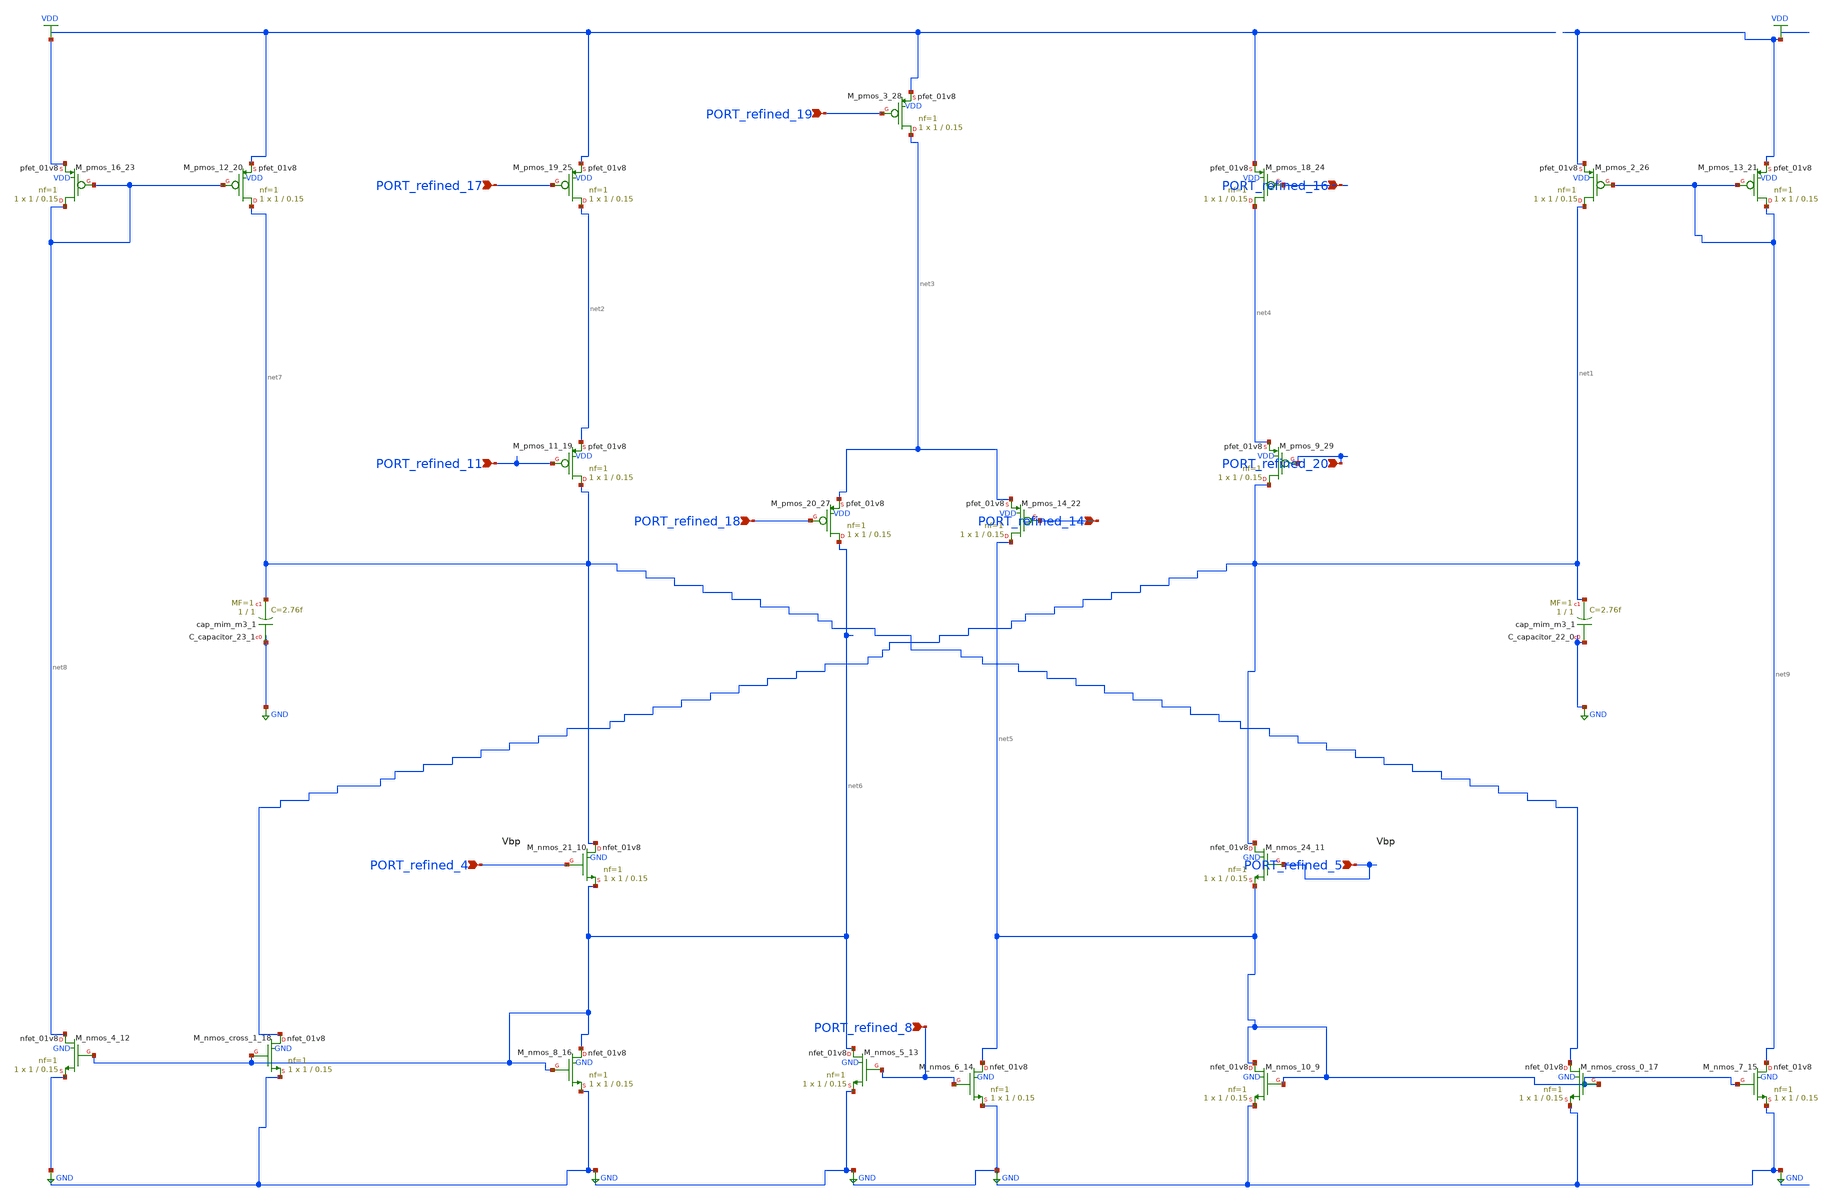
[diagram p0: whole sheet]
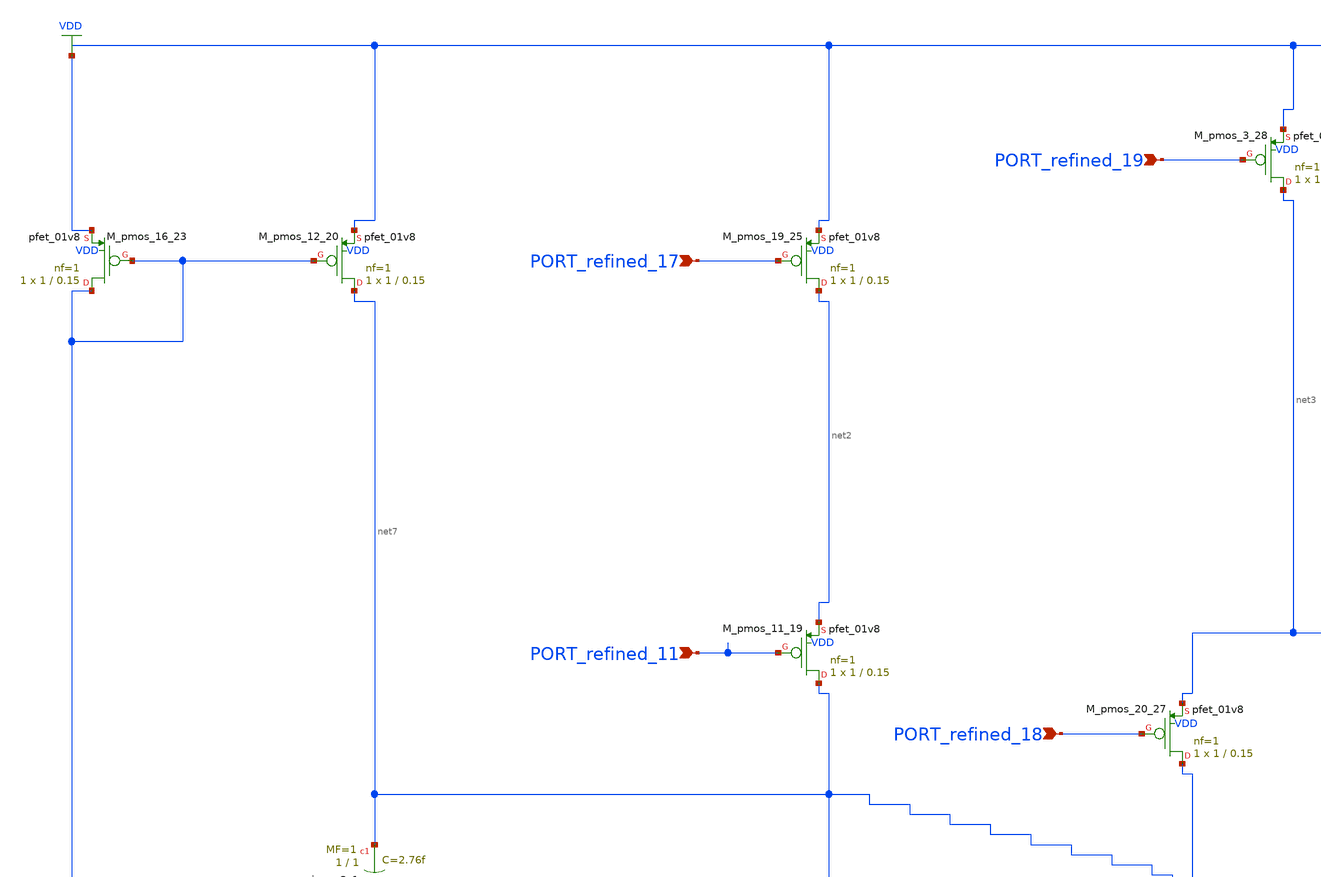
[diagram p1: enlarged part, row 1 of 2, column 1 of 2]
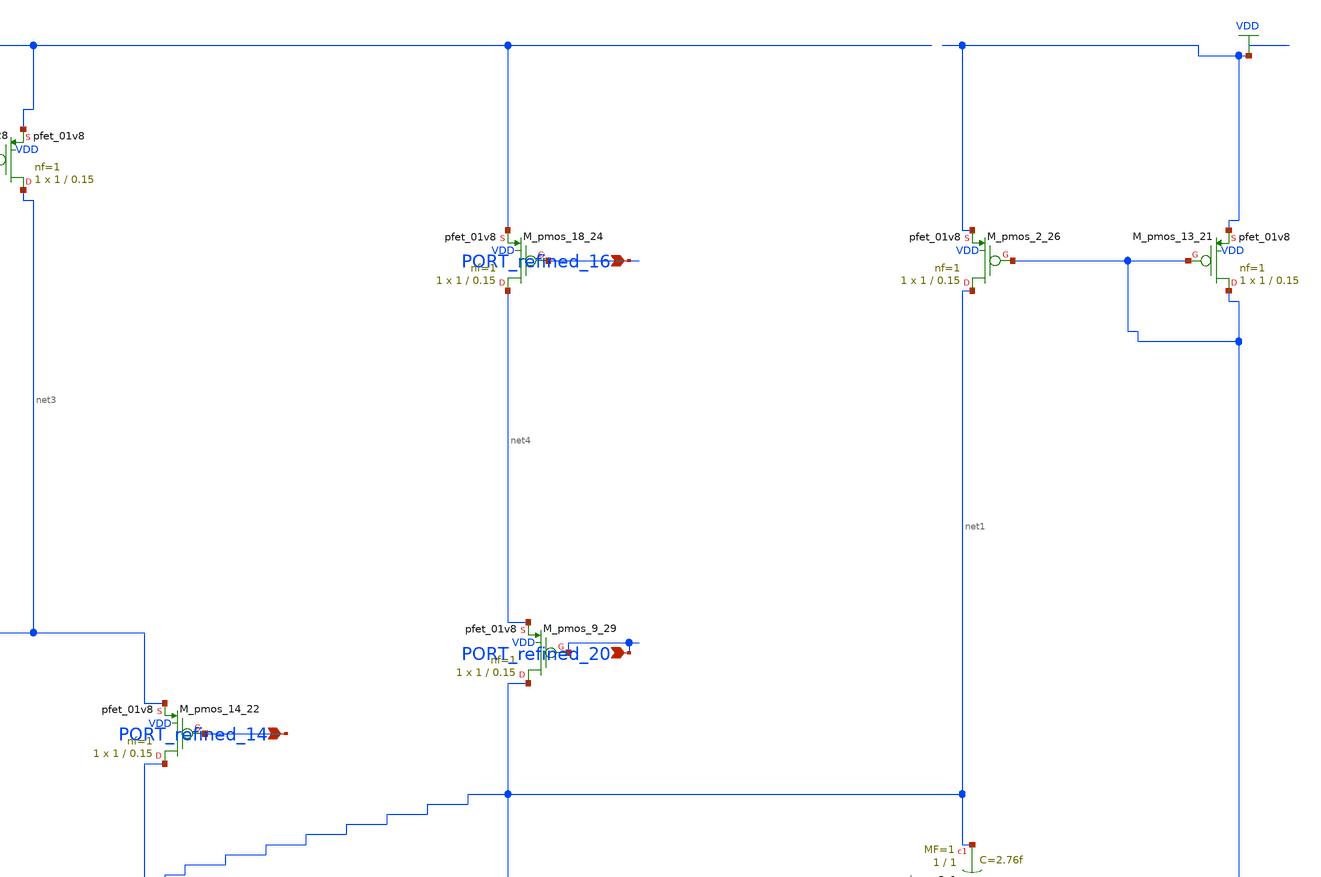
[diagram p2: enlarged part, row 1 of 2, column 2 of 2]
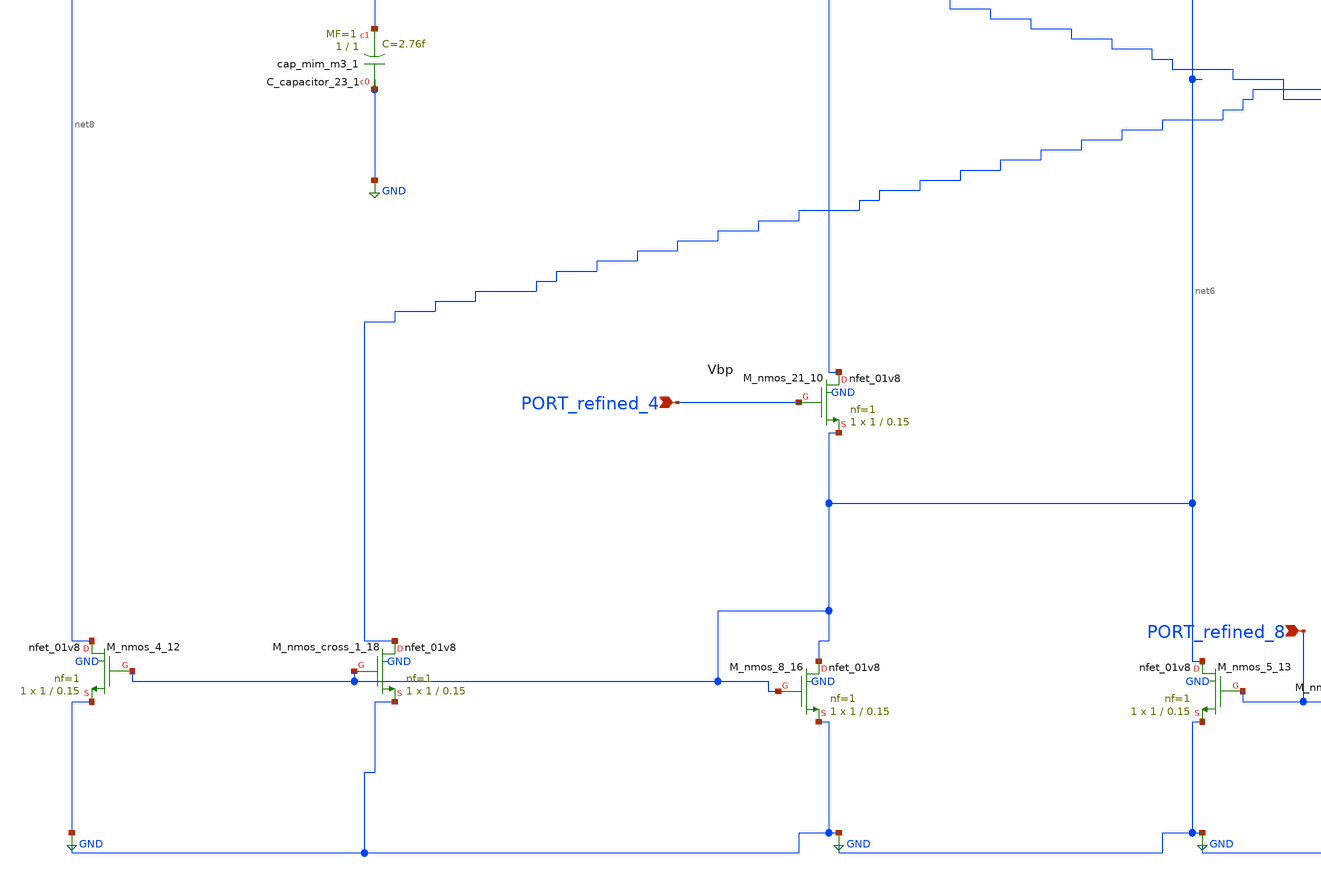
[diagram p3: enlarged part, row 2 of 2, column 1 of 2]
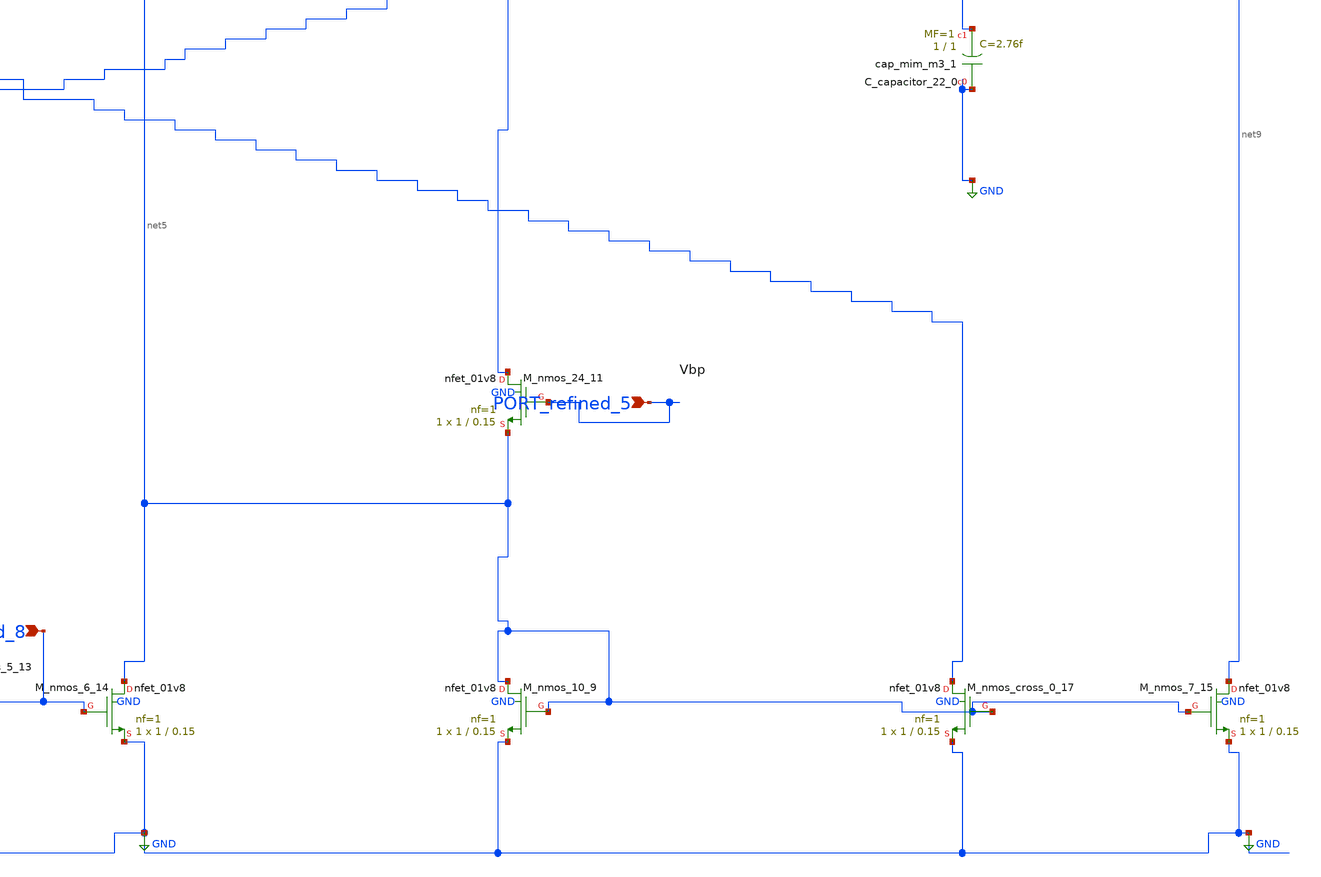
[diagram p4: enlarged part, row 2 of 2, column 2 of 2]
** sch_path: schematics/Image2Net/073.sch
**.subckt 073 PORT_refined_17 PORT_refined_19 PORT_refined_18 PORT_refined_16 PORT_refined_8
*+ PORT_refined_11 PORT_refined_14 PORT_refined_20 PORT_refined_4 PORT_refined_5
*.ipin PORT_refined_17
*.ipin PORT_refined_19
*.ipin PORT_refined_18
*.ipin PORT_refined_16
*.ipin PORT_refined_8
*.ipin PORT_refined_11
*.ipin PORT_refined_14
*.ipin PORT_refined_20
*.ipin PORT_refined_4
*.ipin PORT_refined_5
XC_capacitor_22_0 GND net1 sky130_fd_pr__cap_mim_m3_1 W=1 L=1 MF=1 m=1
XC_capacitor_23_1 GND net7 sky130_fd_pr__cap_mim_m3_1 W=1 L=1 MF=1 m=1
XM_nmos_10_9 net5 net5 GND GND sky130_fd_pr__nfet_01v8 L=0.15 W=1 nf=1 ad='int((1 + 1)/2) * 1 / 1 * 0.29'
+ as='int((1 + 2)/2) * 1 / 1 * 0.29' pd='2*int((1 + 1)/2) * (1 / 1 + 0.29)' ps='2*int((1 + 2)/2) * (1 / 1 + 0.29)'
+ nrd='0.29 / 1 ' nrs='0.29 / 1 ' sa=0 sb=0 sd=0 mult=1 m=1
XM_nmos_21_10 net7 PORT_refined_4 net6 GND sky130_fd_pr__nfet_01v8 L=0.15 W=1 nf=1 ad='int((1 + 1)/2) * 1 / 1 * 0.29'
+ as='int((1 + 2)/2) * 1 / 1 * 0.29' pd='2*int((1 + 1)/2) * (1 / 1 + 0.29)' ps='2*int((1 + 2)/2) * (1 / 1 + 0.29)'
+ nrd='0.29 / 1 ' nrs='0.29 / 1 ' sa=0 sb=0 sd=0 mult=1 m=1
XM_nmos_24_11 net1 PORT_refined_5 net5 GND sky130_fd_pr__nfet_01v8 L=0.15 W=1 nf=1 ad='int((1 + 1)/2) * 1 / 1 * 0.29'
+ as='int((1 + 2)/2) * 1 / 1 * 0.29' pd='2*int((1 + 1)/2) * (1 / 1 + 0.29)' ps='2*int((1 + 2)/2) * (1 / 1 + 0.29)'
+ nrd='0.29 / 1 ' nrs='0.29 / 1 ' sa=0 sb=0 sd=0 mult=1 m=1
XM_nmos_4_12 net8 net6 GND GND sky130_fd_pr__nfet_01v8 L=0.15 W=1 nf=1 ad='int((1 + 1)/2) * 1 / 1 * 0.29'
+ as='int((1 + 2)/2) * 1 / 1 * 0.29' pd='2*int((1 + 1)/2) * (1 / 1 + 0.29)' ps='2*int((1 + 2)/2) * (1 / 1 + 0.29)'
+ nrd='0.29 / 1 ' nrs='0.29 / 1 ' sa=0 sb=0 sd=0 mult=1 m=1
XM_nmos_5_13 net6 PORT_refined_8 GND GND sky130_fd_pr__nfet_01v8 L=0.15 W=1 nf=1 ad='int((1 + 1)/2) * 1 / 1 * 0.29'
+ as='int((1 + 2)/2) * 1 / 1 * 0.29' pd='2*int((1 + 1)/2) * (1 / 1 + 0.29)' ps='2*int((1 + 2)/2) * (1 / 1 + 0.29)'
+ nrd='0.29 / 1 ' nrs='0.29 / 1 ' sa=0 sb=0 sd=0 mult=1 m=1
XM_nmos_6_14 net5 PORT_refined_8 GND GND sky130_fd_pr__nfet_01v8 L=0.15 W=1 nf=1 ad='int((1 + 1)/2) * 1 / 1 * 0.29'
+ as='int((1 + 2)/2) * 1 / 1 * 0.29' pd='2*int((1 + 1)/2) * (1 / 1 + 0.29)' ps='2*int((1 + 2)/2) * (1 / 1 + 0.29)'
+ nrd='0.29 / 1 ' nrs='0.29 / 1 ' sa=0 sb=0 sd=0 mult=1 m=1
XM_nmos_7_15 net9 net5 GND GND sky130_fd_pr__nfet_01v8 L=0.15 W=1 nf=1 ad='int((1 + 1)/2) * 1 / 1 * 0.29'
+ as='int((1 + 2)/2) * 1 / 1 * 0.29' pd='2*int((1 + 1)/2) * (1 / 1 + 0.29)' ps='2*int((1 + 2)/2) * (1 / 1 + 0.29)'
+ nrd='0.29 / 1 ' nrs='0.29 / 1 ' sa=0 sb=0 sd=0 mult=1 m=1
XM_nmos_8_16 net6 net6 GND GND sky130_fd_pr__nfet_01v8 L=0.15 W=1 nf=1 ad='int((1 + 1)/2) * 1 / 1 * 0.29'
+ as='int((1 + 2)/2) * 1 / 1 * 0.29' pd='2*int((1 + 1)/2) * (1 / 1 + 0.29)' ps='2*int((1 + 2)/2) * (1 / 1 + 0.29)'
+ nrd='0.29 / 1 ' nrs='0.29 / 1 ' sa=0 sb=0 sd=0 mult=1 m=1
XM_nmos_cross_0_17 net7 net5 GND GND sky130_fd_pr__nfet_01v8 L=0.15 W=1 nf=1 ad='int((1 + 1)/2) * 1 / 1 * 0.29'
+ as='int((1 + 2)/2) * 1 / 1 * 0.29' pd='2*int((1 + 1)/2) * (1 / 1 + 0.29)' ps='2*int((1 + 2)/2) * (1 / 1 + 0.29)'
+ nrd='0.29 / 1 ' nrs='0.29 / 1 ' sa=0 sb=0 sd=0 mult=1 m=1
XM_nmos_cross_1_18 net1 net6 GND GND sky130_fd_pr__nfet_01v8 L=0.15 W=1 nf=1 ad='int((1 + 1)/2) * 1 / 1 * 0.29'
+ as='int((1 + 2)/2) * 1 / 1 * 0.29' pd='2*int((1 + 1)/2) * (1 / 1 + 0.29)' ps='2*int((1 + 2)/2) * (1 / 1 + 0.29)'
+ nrd='0.29 / 1 ' nrs='0.29 / 1 ' sa=0 sb=0 sd=0 mult=1 m=1
XM_pmos_11_19 net7 PORT_refined_11 net2 VDD sky130_fd_pr__pfet_01v8 L=0.15 W=1 nf=1 ad='int((1 + 1)/2) * 1 / 1 * 0.29'
+ as='int((1 + 2)/2) * 1 / 1 * 0.29' pd='2*int((1 + 1)/2) * (1 / 1 + 0.29)' ps='2*int((1 + 2)/2) * (1 / 1 + 0.29)'
+ nrd='0.29 / 1 ' nrs='0.29 / 1 ' sa=0 sb=0 sd=0 mult=1 m=1
XM_pmos_12_20 net7 net8 VDD VDD sky130_fd_pr__pfet_01v8 L=0.15 W=1 nf=1 ad='int((1 + 1)/2) * 1 / 1 * 0.29'
+ as='int((1 + 2)/2) * 1 / 1 * 0.29' pd='2*int((1 + 1)/2) * (1 / 1 + 0.29)' ps='2*int((1 + 2)/2) * (1 / 1 + 0.29)'
+ nrd='0.29 / 1 ' nrs='0.29 / 1 ' sa=0 sb=0 sd=0 mult=1 m=1
XM_pmos_13_21 net9 net9 VDD VDD sky130_fd_pr__pfet_01v8 L=0.15 W=1 nf=1 ad='int((1 + 1)/2) * 1 / 1 * 0.29'
+ as='int((1 + 2)/2) * 1 / 1 * 0.29' pd='2*int((1 + 1)/2) * (1 / 1 + 0.29)' ps='2*int((1 + 2)/2) * (1 / 1 + 0.29)'
+ nrd='0.29 / 1 ' nrs='0.29 / 1 ' sa=0 sb=0 sd=0 mult=1 m=1
XM_pmos_14_22 net5 PORT_refined_14 net3 VDD sky130_fd_pr__pfet_01v8 L=0.15 W=1 nf=1 ad='int((1 + 1)/2) * 1 / 1 * 0.29'
+ as='int((1 + 2)/2) * 1 / 1 * 0.29' pd='2*int((1 + 1)/2) * (1 / 1 + 0.29)' ps='2*int((1 + 2)/2) * (1 / 1 + 0.29)'
+ nrd='0.29 / 1 ' nrs='0.29 / 1 ' sa=0 sb=0 sd=0 mult=1 m=1
XM_pmos_16_23 net8 net8 VDD VDD sky130_fd_pr__pfet_01v8 L=0.15 W=1 nf=1 ad='int((1 + 1)/2) * 1 / 1 * 0.29'
+ as='int((1 + 2)/2) * 1 / 1 * 0.29' pd='2*int((1 + 1)/2) * (1 / 1 + 0.29)' ps='2*int((1 + 2)/2) * (1 / 1 + 0.29)'
+ nrd='0.29 / 1 ' nrs='0.29 / 1 ' sa=0 sb=0 sd=0 mult=1 m=1
XM_pmos_18_24 net4 PORT_refined_16 VDD VDD sky130_fd_pr__pfet_01v8 L=0.15 W=1 nf=1 ad='int((1 + 1)/2) * 1 / 1 * 0.29'
+ as='int((1 + 2)/2) * 1 / 1 * 0.29' pd='2*int((1 + 1)/2) * (1 / 1 + 0.29)' ps='2*int((1 + 2)/2) * (1 / 1 + 0.29)'
+ nrd='0.29 / 1 ' nrs='0.29 / 1 ' sa=0 sb=0 sd=0 mult=1 m=1
XM_pmos_19_25 net2 PORT_refined_17 VDD VDD sky130_fd_pr__pfet_01v8 L=0.15 W=1 nf=1 ad='int((1 + 1)/2) * 1 / 1 * 0.29'
+ as='int((1 + 2)/2) * 1 / 1 * 0.29' pd='2*int((1 + 1)/2) * (1 / 1 + 0.29)' ps='2*int((1 + 2)/2) * (1 / 1 + 0.29)'
+ nrd='0.29 / 1 ' nrs='0.29 / 1 ' sa=0 sb=0 sd=0 mult=1 m=1
XM_pmos_2_26 net1 net9 VDD VDD sky130_fd_pr__pfet_01v8 L=0.15 W=1 nf=1 ad='int((1 + 1)/2) * 1 / 1 * 0.29'
+ as='int((1 + 2)/2) * 1 / 1 * 0.29' pd='2*int((1 + 1)/2) * (1 / 1 + 0.29)' ps='2*int((1 + 2)/2) * (1 / 1 + 0.29)'
+ nrd='0.29 / 1 ' nrs='0.29 / 1 ' sa=0 sb=0 sd=0 mult=1 m=1
XM_pmos_20_27 net6 PORT_refined_18 net3 VDD sky130_fd_pr__pfet_01v8 L=0.15 W=1 nf=1 ad='int((1 + 1)/2) * 1 / 1 * 0.29'
+ as='int((1 + 2)/2) * 1 / 1 * 0.29' pd='2*int((1 + 1)/2) * (1 / 1 + 0.29)' ps='2*int((1 + 2)/2) * (1 / 1 + 0.29)'
+ nrd='0.29 / 1 ' nrs='0.29 / 1 ' sa=0 sb=0 sd=0 mult=1 m=1
XM_pmos_3_28 net3 PORT_refined_19 VDD VDD sky130_fd_pr__pfet_01v8 L=0.15 W=1 nf=1 ad='int((1 + 1)/2) * 1 / 1 * 0.29'
+ as='int((1 + 2)/2) * 1 / 1 * 0.29' pd='2*int((1 + 1)/2) * (1 / 1 + 0.29)' ps='2*int((1 + 2)/2) * (1 / 1 + 0.29)'
+ nrd='0.29 / 1 ' nrs='0.29 / 1 ' sa=0 sb=0 sd=0 mult=1 m=1
XM_pmos_9_29 net1 PORT_refined_20 net4 VDD sky130_fd_pr__pfet_01v8 L=0.15 W=1 nf=1 ad='int((1 + 1)/2) * 1 / 1 * 0.29'
+ as='int((1 + 2)/2) * 1 / 1 * 0.29' pd='2*int((1 + 1)/2) * (1 / 1 + 0.29)' ps='2*int((1 + 2)/2) * (1 / 1 + 0.29)'
+ nrd='0.29 / 1 ' nrs='0.29 / 1 ' sa=0 sb=0 sd=0 mult=1 m=1
**.ends
.GLOBAL GND
.GLOBAL VDD
.end
